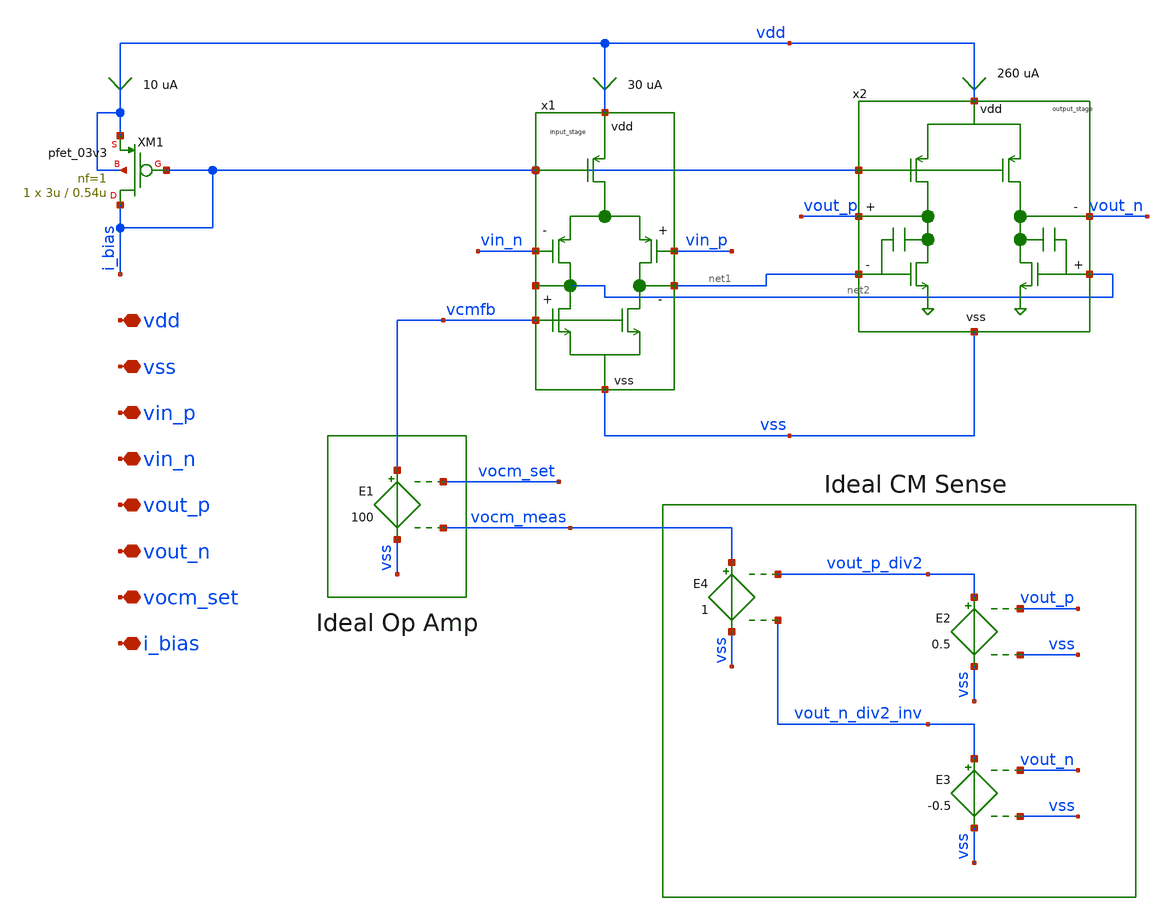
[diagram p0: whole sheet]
** sch_path: xschem/top_level/top_level.sch
**.subckt top_level vdd vss vin_p vin_n vout_p vout_n vocm_set i_bias
*.iopin vdd
*.iopin vss
*.iopin vin_p
*.iopin vin_n
*.iopin vout_p
*.iopin vout_n
*.iopin vocm_set
*.iopin i_bias
x1 vin_p vin_n net2 net1 vdd vss i_bias vcmfb input_stage
x2 vdd vss net2 net1 vout_p vout_n i_bias output_stage
E1 vcmfb vss vocm_set vocm_meas 100
E2 vout_p_div2 vss vout_p vss 0.5
E3 vout_n_div2_inv vss vout_n vss -0.5
E4 vocm_meas vss vout_p_div2 vout_n_div2_inv 1
XM1 i_bias i_bias vdd vdd pfet_03v3 L=0.54u W=3u nf=1 ad='int((nf+1)/2) * W/nf * 0.18u' as='int((nf+2)/2) * W/nf * 0.18u'
+ pd='2*int((nf+1)/2) * (W/nf + 0.18u)' ps='2*int((nf+2)/2) * (W/nf + 0.18u)' nrd='0.18u / W' nrs='0.18u / W'
+ sa=0 sb=0 sd=0 m=1
**.ends
.end
